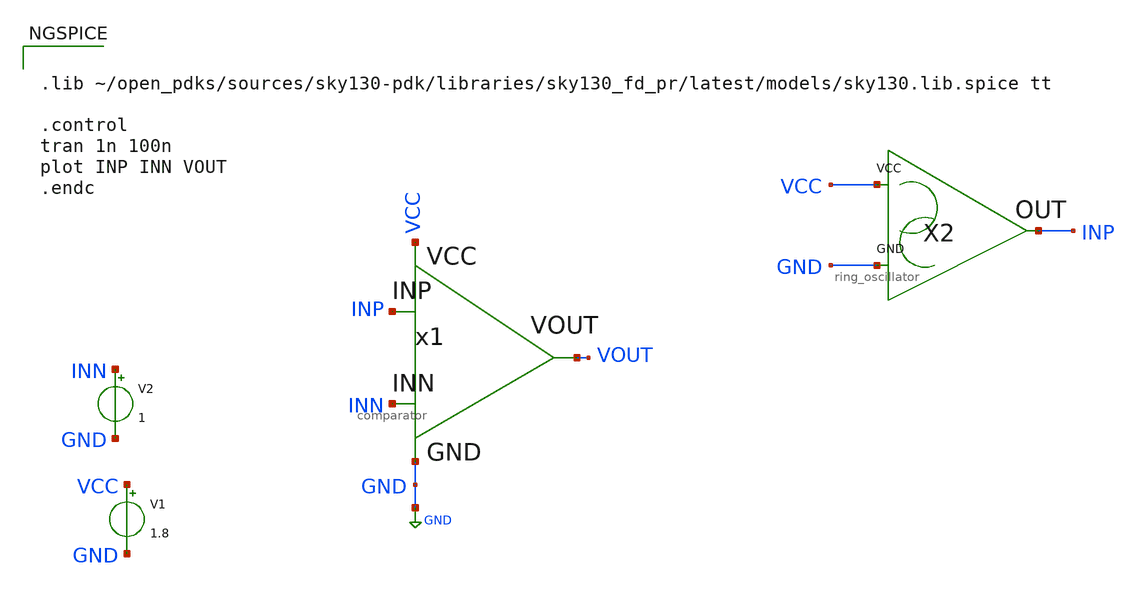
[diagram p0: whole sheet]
** sch_path: Week 4/xschem_comparator/comparator_tb.sch
* Week 4/xschem_comparator/comparator.sch:
* Copyright 2020 Stefan Frederik Schippers
* Licensed under the Apache License, Version 2.0 (the "License");
**.subckt comparator_tb
x1 INN INP VOUT VCC GND comparator
V1 VCC GND 1.8
V2 INN GND 1
X2 GND VCC INP ring_oscillator
**** begin user architecture code


.lib ~/open_pdks/sources/sky130-pdk/libraries/sky130_fd_pr/latest/models/sky130.lib.spice tt

.control
tran 1n 100n
plot INP INN VOUT
.endc


**** end user architecture code
**.ends

* expanding   symbol:  comparator.sym # of pins=5
** sym_path: Week 4/xschem_comparator/comparator.sym
** sch_path: Week 4/xschem_comparator/comparator.sch
.subckt comparator INN INP VOUT VCC GND
*.iopin VCC
*.iopin GND
*.opin VOUT
*.ipin INP
*.ipin INN
Ihyst VCC net4 pwl 0 0 20u 0 21u 0.2u 40u 0.2u 41u 0.8u 60u 0.8u 61u 10u 100u 10u
LOAD VOUT GND 10M m=1
XM1 net1 net1 VCC VCC sky130_fd_pr__pfet_01v8 L=1 W=1 nf=1 ad='int((nf+1)/2) * W/nf * 0.29' as='int((nf+2)/2) * W/nf * 0.29'
+ pd='2*int((nf+1)/2) * (W/nf + 0.29)' ps='2*int((nf+2)/2) * (W/nf + 0.29)' nrd='0.29 / W' nrs='0.29 / W'
+ sa=0 sb=0 sd=0 mult=1 m=1
XM2 VDIFF net1 VCC VCC sky130_fd_pr__pfet_01v8 L=1 W=1 nf=1 ad='int((nf+1)/2) * W/nf * 0.29' as='int((nf+2)/2) * W/nf * 0.29'
+ pd='2*int((nf+1)/2) * (W/nf + 0.29)' ps='2*int((nf+2)/2) * (W/nf + 0.29)' nrd='0.29 / W' nrs='0.29 / W'
+ sa=0 sb=0 sd=0 mult=1 m=1
XM9 VOUT1 VDIFF VCC VCC sky130_fd_pr__pfet_01v8 L=0.5 W=6 nf=1 ad='int((nf+1)/2) * W/nf * 0.29' as='int((nf+2)/2) * W/nf * 0.29'
+ pd='2*int((nf+1)/2) * (W/nf + 0.29)' ps='2*int((nf+2)/2) * (W/nf + 0.29)' nrd='0.29 / W' nrs='0.29 / W'
+ sa=0 sb=0 sd=0 mult=1 m=1
XM10 VOUT2 VCC VCC VCC sky130_fd_pr__pfet_01v8 L=0.5 W=4 nf=1 ad='int((nf+1)/2) * W/nf * 0.29' as='int((nf+2)/2) * W/nf * 0.29'
+ pd='2*int((nf+1)/2) * (W/nf + 0.29)' ps='2*int((nf+2)/2) * (W/nf + 0.29)' nrd='0.29 / W' nrs='0.29 / W'
+ sa=0 sb=0 sd=0 mult=1 m=1
XM12 VOUT2 VOUT1 VCC VCC sky130_fd_pr__pfet_01v8 L=0.5 W=4 nf=1 ad='int((nf+1)/2) * W/nf * 0.29' as='int((nf+2)/2) * W/nf * 0.29'
+ pd='2*int((nf+1)/2) * (W/nf + 0.29)' ps='2*int((nf+2)/2) * (W/nf + 0.29)' nrd='0.29 / W' nrs='0.29 / W'
+ sa=0 sb=0 sd=0 mult=1 m=1
XM14 VOUT VOUT2 VCC VCC sky130_fd_pr__pfet_01v8 L=0.5 W=4 nf=1 ad='int((nf+1)/2) * W/nf * 0.29' as='int((nf+2)/2) * W/nf * 0.29'
+ pd='2*int((nf+1)/2) * (W/nf + 0.29)' ps='2*int((nf+2)/2) * (W/nf + 0.29)' nrd='0.29 / W' nrs='0.29 / W'
+ sa=0 sb=0 sd=0 mult=1 m=1
XM3 net1 INN net2 GND sky130_fd_pr__nfet_01v8 L=0.5 W=1 nf=1 ad='int((nf+1)/2) * W/nf * 0.29' as='int((nf+2)/2) * W/nf * 0.29'
+ pd='2*int((nf+1)/2) * (W/nf + 0.29)' ps='2*int((nf+2)/2) * (W/nf + 0.29)' nrd='0.29 / W' nrs='0.29 / W'
+ sa=0 sb=0 sd=0 mult=1 m=1
XM4 VDIFF INP net2 GND sky130_fd_pr__nfet_01v8 L=0.5 W=1 nf=1 ad='int((nf+1)/2) * W/nf * 0.29' as='int((nf+2)/2) * W/nf * 0.29'
+ pd='2*int((nf+1)/2) * (W/nf + 0.29)' ps='2*int((nf+2)/2) * (W/nf + 0.29)' nrd='0.29 / W' nrs='0.29 / W'
+ sa=0 sb=0 sd=0 mult=1 m=1
XM5 net2 VCC GND GND sky130_fd_pr__nfet_01v8 L=1 W=0.5 nf=1 ad='int((nf+1)/2) * W/nf * 0.29' as='int((nf+2)/2) * W/nf * 0.29'
+ pd='2*int((nf+1)/2) * (W/nf + 0.29)' ps='2*int((nf+2)/2) * (W/nf + 0.29)' nrd='0.29 / W' nrs='0.29 / W'
+ sa=0 sb=0 sd=0 mult=1 m=1
XM15 net4 net4 GND GND sky130_fd_pr__nfet_01v8 L=0.5 W=0.5 nf=1 ad='int((nf+1)/2) * W/nf * 0.29' as='int((nf+2)/2) * W/nf * 0.29'
+ pd='2*int((nf+1)/2) * (W/nf + 0.29)' ps='2*int((nf+2)/2) * (W/nf + 0.29)' nrd='0.29 / W' nrs='0.29 / W'
+ sa=0 sb=0 sd=0 mult=1 m=1
XM7 net3 net4 GND GND sky130_fd_pr__nfet_01v8 L=0.5 W=0.5 nf=1 ad='int((nf+1)/2) * W/nf * 0.29' as='int((nf+2)/2) * W/nf * 0.29'
+ pd='2*int((nf+1)/2) * (W/nf + 0.29)' ps='2*int((nf+2)/2) * (W/nf + 0.29)' nrd='0.29 / W' nrs='0.29 / W'
+ sa=0 sb=0 sd=0 mult=1 m=1
XM11 VOUT1 VCC GND GND sky130_fd_pr__nfet_01v8 L=0.5 W=0.5 nf=1 ad='int((nf+1)/2) * W/nf * 0.29' as='int((nf+2)/2) * W/nf * 0.29'
+ pd='2*int((nf+1)/2) * (W/nf + 0.29)' ps='2*int((nf+2)/2) * (W/nf + 0.29)' nrd='0.29 / W' nrs='0.29 / W'
+ sa=0 sb=0 sd=0 mult=1 m=1
XM6 net1 VOUT2 net3 GND sky130_fd_pr__nfet_01v8 L=0.5 W=2 nf=1 ad='int((nf+1)/2) * W/nf * 0.29' as='int((nf+2)/2) * W/nf * 0.29'
+ pd='2*int((nf+1)/2) * (W/nf + 0.29)' ps='2*int((nf+2)/2) * (W/nf + 0.29)' nrd='0.29 / W' nrs='0.29 / W'
+ sa=0 sb=0 sd=0 mult=1 m=1
XM8 VDIFF VOUT1 net3 GND sky130_fd_pr__nfet_01v8 L=0.5 W=2 nf=1 ad='int((nf+1)/2) * W/nf * 0.29' as='int((nf+2)/2) * W/nf * 0.29'
+ pd='2*int((nf+1)/2) * (W/nf + 0.29)' ps='2*int((nf+2)/2) * (W/nf + 0.29)' nrd='0.29 / W' nrs='0.29 / W'
+ sa=0 sb=0 sd=0 mult=1 m=1
XM13 VOUT2 VOUT1 net5 GND sky130_fd_pr__nfet_01v8 L=0.5 W=2 nf=1 ad='int((nf+1)/2) * W/nf * 0.29' as='int((nf+2)/2) * W/nf * 0.29'
+ pd='2*int((nf+1)/2) * (W/nf + 0.29)' ps='2*int((nf+2)/2) * (W/nf + 0.29)' nrd='0.29 / W' nrs='0.29 / W'
+ sa=0 sb=0 sd=0 mult=1 m=1
XM16 net5 VCC GND GND sky130_fd_pr__nfet_01v8 L=0.5 W=2 nf=1 ad='int((nf+1)/2) * W/nf * 0.29' as='int((nf+2)/2) * W/nf * 0.29'
+ pd='2*int((nf+1)/2) * (W/nf + 0.29)' ps='2*int((nf+2)/2) * (W/nf + 0.29)' nrd='0.29 / W' nrs='0.29 / W'
+ sa=0 sb=0 sd=0 mult=1 m=1
XM17 VOUT VOUT2 GND GND sky130_fd_pr__nfet_01v8 L=0.5 W=2 nf=1 ad='int((nf+1)/2) * W/nf * 0.29' as='int((nf+2)/2) * W/nf * 0.29'
+ pd='2*int((nf+1)/2) * (W/nf + 0.29)' ps='2*int((nf+2)/2) * (W/nf + 0.29)' nrd='0.29 / W' nrs='0.29 / W'
+ sa=0 sb=0 sd=0 mult=1 m=1
.ends


* expanding   symbol:  ring_oscillator.sym # of pins=3
** sym_path: Week 4/xschem_comparator/ring_oscillator.sym
** sch_path: Week 4/xschem_comparator/ring_oscillator.sch
.subckt ring_oscillator GND VCC OUT
*.opin OUT
*.iopin VCC
*.iopin GND
XM1 net1 OUT VCC VCC sky130_fd_pr__pfet_01v8 L=0.15 W=1.68 nf=1 ad='int((nf+1)/2) * W/nf * 0.29' as='int((nf+2)/2) * W/nf * 0.29'
+ pd='2*int((nf+1)/2) * (W/nf + 0.29)' ps='2*int((nf+2)/2) * (W/nf + 0.29)' nrd='0.29 / W' nrs='0.29 / W'
+ sa=0 sb=0 sd=0 mult=1 m=1
XM2 net2 net1 VCC VCC sky130_fd_pr__pfet_01v8 L=0.15 W=1.68 nf=1 ad='int((nf+1)/2) * W/nf * 0.29' as='int((nf+2)/2) * W/nf * 0.29'
+ pd='2*int((nf+1)/2) * (W/nf + 0.29)' ps='2*int((nf+2)/2) * (W/nf + 0.29)' nrd='0.29 / W' nrs='0.29 / W'
+ sa=0 sb=0 sd=0 mult=1 m=1
XM3 OUT net2 VCC VCC sky130_fd_pr__pfet_01v8 L=0.15 W=1.68 nf=1 ad='int((nf+1)/2) * W/nf * 0.29' as='int((nf+2)/2) * W/nf * 0.29'
+ pd='2*int((nf+1)/2) * (W/nf + 0.29)' ps='2*int((nf+2)/2) * (W/nf + 0.29)' nrd='0.29 / W' nrs='0.29 / W'
+ sa=0 sb=0 sd=0 mult=1 m=1
XM4 net1 OUT GND GND sky130_fd_pr__nfet_01v8 L=0.15 W=1.68 nf=1 ad='int((nf+1)/2) * W/nf * 0.29' as='int((nf+2)/2) * W/nf * 0.29'
+ pd='2*int((nf+1)/2) * (W/nf + 0.29)' ps='2*int((nf+2)/2) * (W/nf + 0.29)' nrd='0.29 / W' nrs='0.29 / W'
+ sa=0 sb=0 sd=0 mult=1 m=1
XM5 net2 net1 GND GND sky130_fd_pr__nfet_01v8 L=0.15 W=1.68 nf=1 ad='int((nf+1)/2) * W/nf * 0.29' as='int((nf+2)/2) * W/nf * 0.29'
+ pd='2*int((nf+1)/2) * (W/nf + 0.29)' ps='2*int((nf+2)/2) * (W/nf + 0.29)' nrd='0.29 / W' nrs='0.29 / W'
+ sa=0 sb=0 sd=0 mult=1 m=1
XM6 OUT net2 GND GND sky130_fd_pr__nfet_01v8 L=0.15 W=1.68 nf=1 ad='int((nf+1)/2) * W/nf * 0.29' as='int((nf+2)/2) * W/nf * 0.29'
+ pd='2*int((nf+1)/2) * (W/nf + 0.29)' ps='2*int((nf+2)/2) * (W/nf + 0.29)' nrd='0.29 / W' nrs='0.29 / W'
+ sa=0 sb=0 sd=0 mult=1 m=1
.ends

.GLOBAL GND
.end
